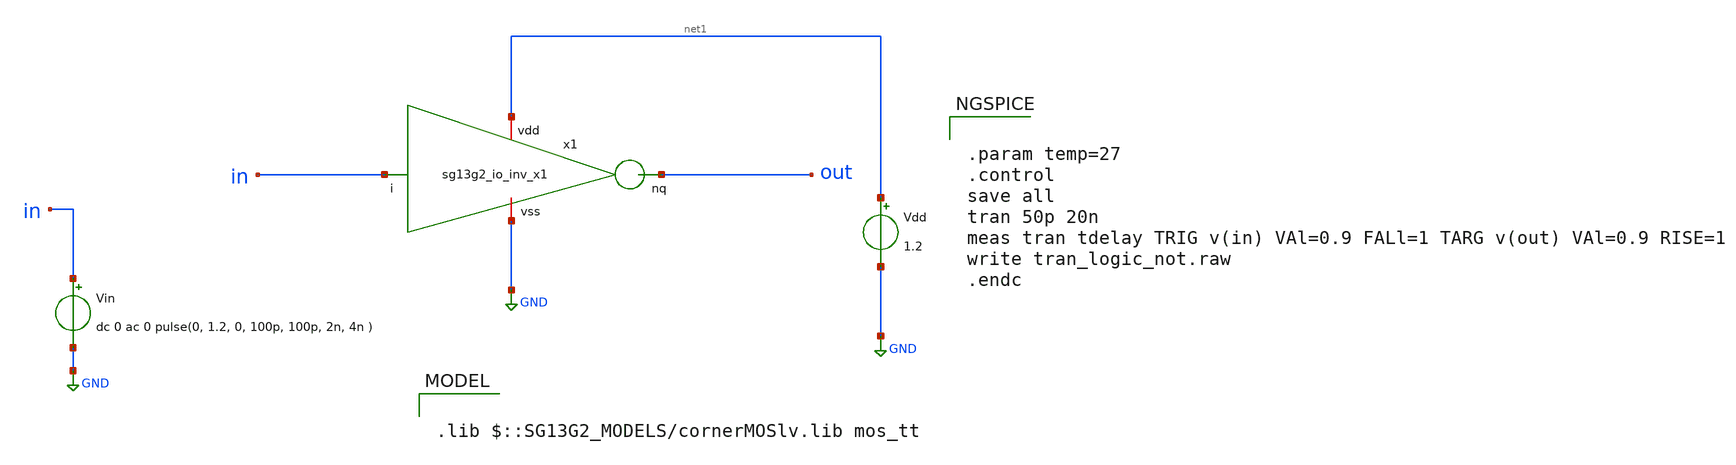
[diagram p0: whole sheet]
** sch_path: ihp-sg13g2/libs.ref/sg13g2_io/xschem/io_testbench/sg13g2_io_inv_x1_tb.sch
* Copyright 2023 IHP PDK Authors
**.subckt sg13g2_io_inv_x1_tb
Vin in GND dc 0 ac 0 pulse(0, 1.2, 0, 100p, 100p, 2n, 4n )
Vdd net1 GND 1.2
x1 net1 in out GND sg13g2_io_inv_x1
**** begin user architecture code

.lib $::SG13G2_MODELS/cornerMOSlv.lib mos_tt



.param temp=27
.control
save all
tran 50p 20n
meas tran tdelay TRIG v(in) VAl=0.9 FALl=1 TARG v(out) VAl=0.9 RISE=1
write tran_logic_not.raw
.endc


**** end user architecture code
**.ends

* expanding   symbol:  sg13g2_io_inv_x1.sym # of pins=4
** sym_path: ihp-sg13g2/libs.ref/sg13g2_io/xschem/sg13g2_io_inv_x1.sym
** sch_path: ihp-sg13g2/libs.ref/sg13g2_io/xschem/sg13g2_io_inv_x1.sch
.subckt sg13g2_io_inv_x1 vdd i nq vss
*.ipin i
*.iopin vdd
*.iopin vss
*.opin nq
XM2 nq i vdd vdd sg13_lv_pmos w=4.41u l=0.13u ng=1 m=1 mm_ok=1
XM1 vss i nq vss sg13_lv_nmos w=3.93u l=0.13u ng=1 m=1 mm_ok=1
.ends

.GLOBAL GND
.end
